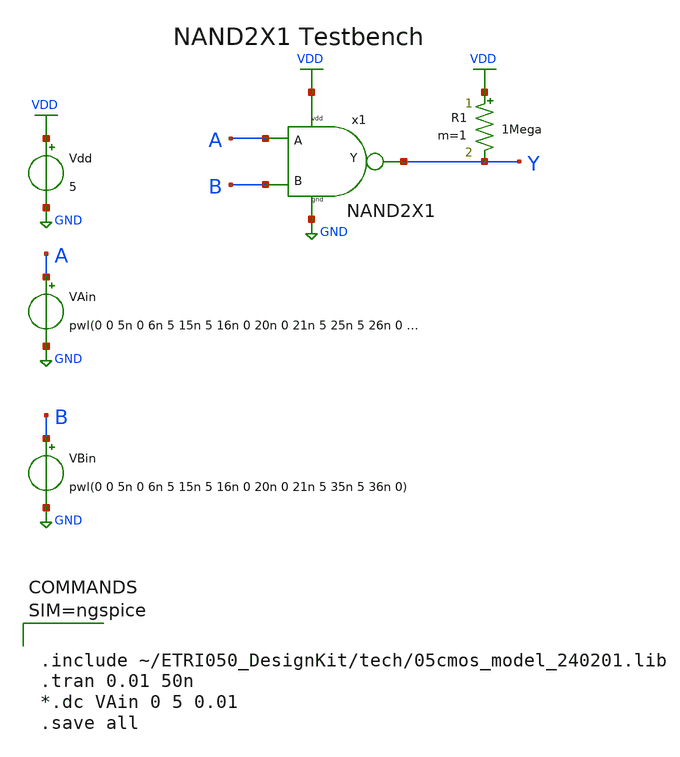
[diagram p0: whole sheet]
** sch_path: Tutorials/1-4_StdCell_DFFSR/Sch/NAND2X1_TB.sch
**.subckt NAND2X1_TB
Vdd VDD GND 5
VAin A GND pwl(0 0 5n 0 6n 5 15n 5 16n 0 20n 0 21n 5 25n 5 26n 0 30n 0 31n 5 40n 5 41n 0)
R1 VDD Y 1Mega m=1
x1 A B Y VDD GND NAND2X1
VBin B GND pwl(0 0 5n 0 6n 5 15n 5 16n 0 20n 0 21n 5 35n 5 36n 0)
**** begin user architecture code



.include ~/ETRI050_DesignKit/tech/05cmos_model_240201.lib
.tran 0.01 50n
*.dc VAin 0 5 0.01
.save all



**** end user architecture code
**.ends

* expanding   symbol:  /home/goodkook/ETRI050_DesignKit/Tutorials/1-4_StdCell_DFFSR/Sch/NAND2X1.sym
*+ # of pins=5
** sym_path: Tutorials/1-4_StdCell_DFFSR/Sch/NAND2X1.sym
** sch_path: Tutorials/1-4_StdCell_DFFSR/Sch/NAND2X1.sch
.subckt NAND2X1 A B Y vdd gnd
*.ipin A
*.ipin B
*.opin Y
*.iopin vdd
*.iopin gnd
M1 Y B net1 GND nfet w=6u l=0.6u m=1
M2 Y B vdd VDD pfet w=6u l=0.6u m=1
M3 net1 A gnd GND nfet w=6u l=0.6u m=1
M4 Y A vdd VDD pfet w=6u l=0.6u m=1
.ends

.GLOBAL VDD
.GLOBAL GND
.end
